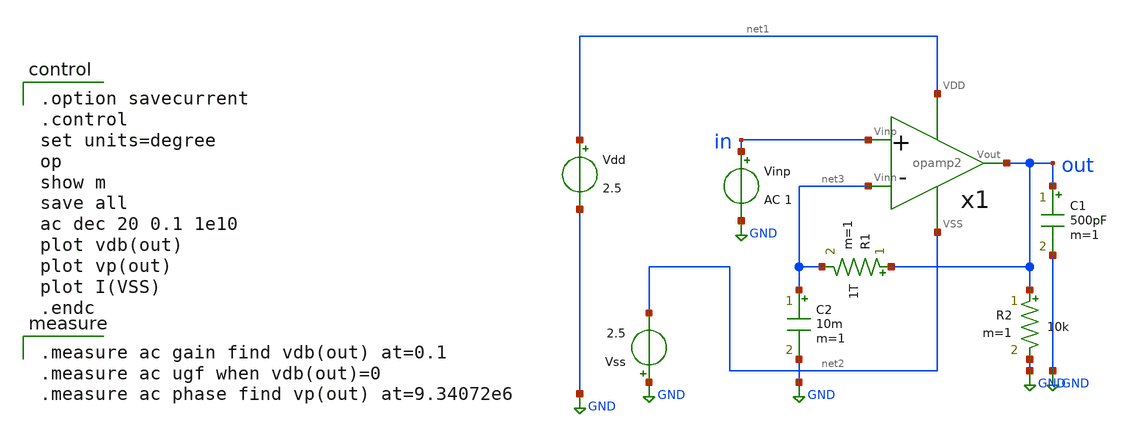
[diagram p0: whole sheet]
** sch_path: OPAF2026/opamp_ac.sch
**.subckt opamp_ac
Vdd net1 GND 2.5
Vinp in GND AC 1
C1 out GND 500pF m=1
R1 out net3 1T m=1
C2 net3 GND 10m m=1
Vss GND net2 2.5
R2 out GND 10k m=1
x1 in net3 out net1 net2 opamp2
**** begin user architecture code

.option savecurrent
.control
set units=degree
op
show m
save all
ac dec 20 0.1 1e10
plot vdb(out)
plot vp(out)
plot I(VSS)
.endc


.measure ac gain find vdb(out) at=0.1
.measure ac ugf when vdb(out)=0
.measure ac phase find vp(out) at=9.34072e6

 .include $::LIB/ip62_models
**** end user architecture code
**.ends

* expanding   symbol:  /home/tsukiji_lab04/OPAF2026/opamp2.sym # of pins=5
** sym_path: OPAF2026/opamp2.sym
** sch_path: OPAF2026/opamp2.sch
.subckt opamp2 Vinp Vinn Vout VDD VSS
*.opin Vout
*.iopin VDD
*.iopin VSS
*.ipin Vinn
*.ipin Vinp
XXM1 net2 net1 VDD VDD PMOS w=50u l=1u nrd=0 nrs=0 m=1
XXM2 net1 net1 VDD VDD PMOS w=50u l=1u nrd=0 nrs=0 m=1
XXM3 net1 Vinn net3 VSS NMOS w=115u l=1u nrd=0 nrs=0 m=1
XXM4 net2 Vinp net3 VSS NMOS w=115u l=1u nrd=0 nrs=0 m=1
XXM5 Vout net2 VDD VDD PMOS w=1360u l=1u nrd=0 nrs=0 m=1
XXM6 net3 net4 VSS VSS NMOS w=175u l=1u nrd=0 nrs=0 m=1
XXM7 Vout net4 VSS VSS NMOS w=2440u l=1u nrd=0 nrs=0 m=1
XXM8 net4 net4 VSS VSS NMOS w=200u l=10u nrd=0 nrs=0 m=1
C1 net5 Vout 25p m=1
R1 VDD net4 58.70k m=1
R2 net2 net5 1k m=1
.ends

.GLOBAL GND
.end
